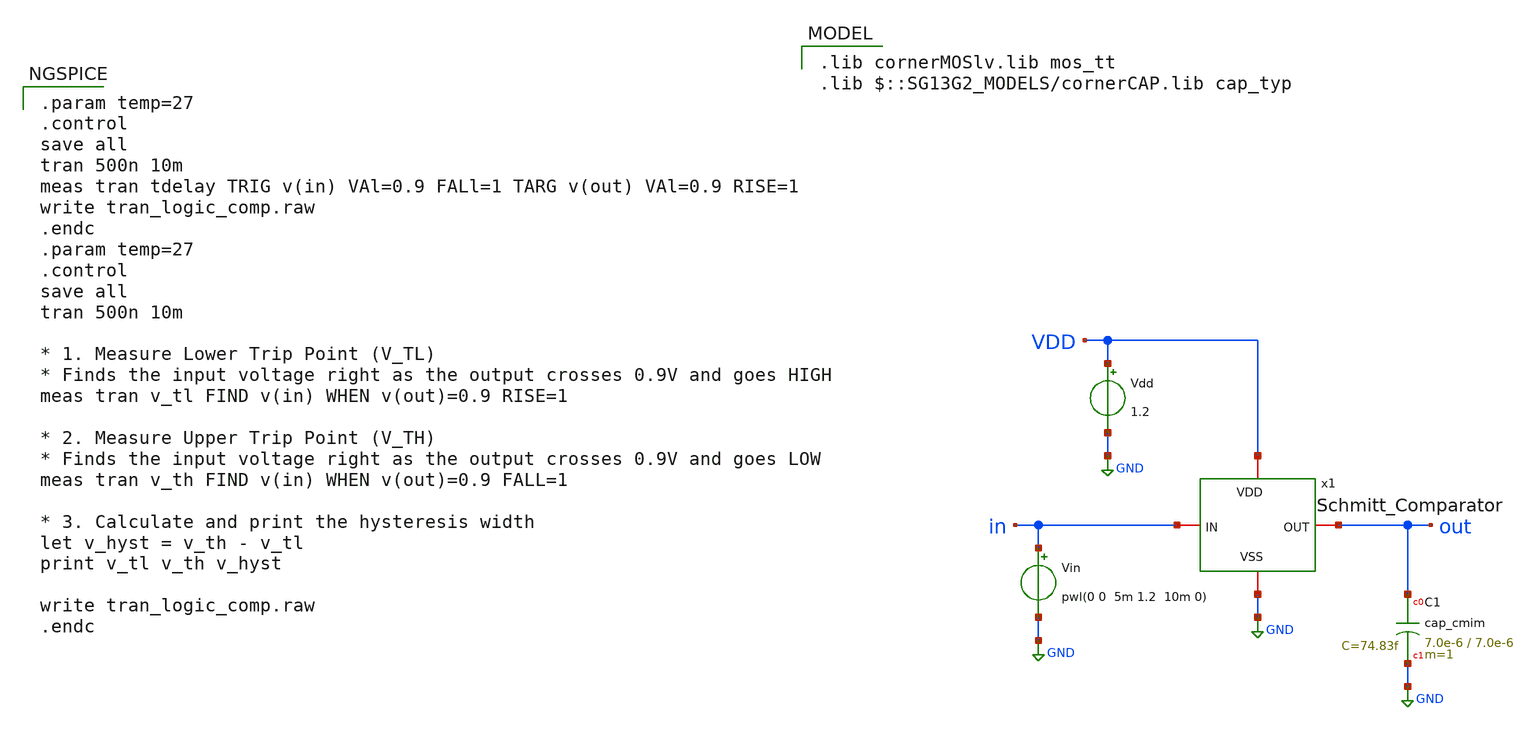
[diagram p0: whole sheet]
** sch_path: xschem/Comparator_tb.sch
**.subckt Comparator_tb
Vdd VDD GND 1.2
XC1 out GND cap_cmim w=7.0e-6 l=7.0e-6 m=1 mm_ok=1
x1 GND VDD in out Schmitt_Comparator
Vin in GND pwl(0 0 5m 1.2 10m 0)
**** begin user architecture code
 .lib cornerMOSlv.lib mos_tt
.lib $::SG13G2_MODELS/cornerCAP.lib cap_typ


.param temp=27
.control
save all
tran 500n 10m
meas tran tdelay TRIG v(in) VAl=0.9 FALl=1 TARG v(out) VAl=0.9 RISE=1
write tran_logic_comp.raw
.endc
.param temp=27
.control
save all
tran 500n 10m

* 1. Measure Lower Trip Point (V_TL)
* Finds the input voltage right as the output crosses 0.9V and goes HIGH
meas tran v_tl FIND v(in) WHEN v(out)=0.9 RISE=1

* 2. Measure Upper Trip Point (V_TH)
* Finds the input voltage right as the output crosses 0.9V and goes LOW
meas tran v_th FIND v(in) WHEN v(out)=0.9 FALL=1

* 3. Calculate and print the hysteresis width
let v_hyst = v_th - v_tl
print v_tl v_th v_hyst

write tran_logic_comp.raw
.endc

**** end user architecture code
**.ends

* expanding   symbol:  /headless/eda/Hall_Xschem_Logic/Schmitt_Comparator.sym # of pins=4
** sym_path: xschem/Schmitt_Comparator.sym
** sch_path: xschem/Schmitt_Comparator.sch
.subckt Schmitt_Comparator VSS VDD IN OUT
*.iopin VSS
*.iopin VDD
*.iopin OUT
*.iopin IN
XM1 net1 IN VDD VDD sg13_lv_pmos w=2u l=0.13u ng=1 m=1 mm_ok=1
XM2 net2 IN net1 VDD sg13_lv_pmos w=2u l=0.13u ng=1 m=1 mm_ok=1
XM3 net2 IN net3 VSS sg13_lv_nmos w=4u l=0.13u ng=1 m=1 mm_ok=1
XM4 net3 IN VSS VSS sg13_lv_nmos w=4u l=0.13u ng=1 m=1 mm_ok=1
XM5 VSS net2 net1 VDD sg13_lv_pmos w=1u l=2u ng=1 m=1 mm_ok=1
XM6 VDD net2 net3 VSS sg13_lv_nmos w=0.5u l=2u ng=1 m=1 mm_ok=1
XC1 IN VSS cap_cmim w=2e-6 l=2e-6 m=1 mm_ok=1
XC18 OUT VSS cap_cmim w=5e-6 l=5e-6 m=1 mm_ok=1
XM7 OUT net2 VDD VDD sg13_lv_pmos w=2u l=0.13u ng=1 m=1 mm_ok=1
XM8 OUT net2 VSS VSS sg13_lv_nmos w=1u l=0.13u ng=1 m=1 mm_ok=1
XC2 net2 VSS cap_cmim w=4e-6 l=4e-6 m=1 mm_ok=1
.ends

.GLOBAL GND
.end
